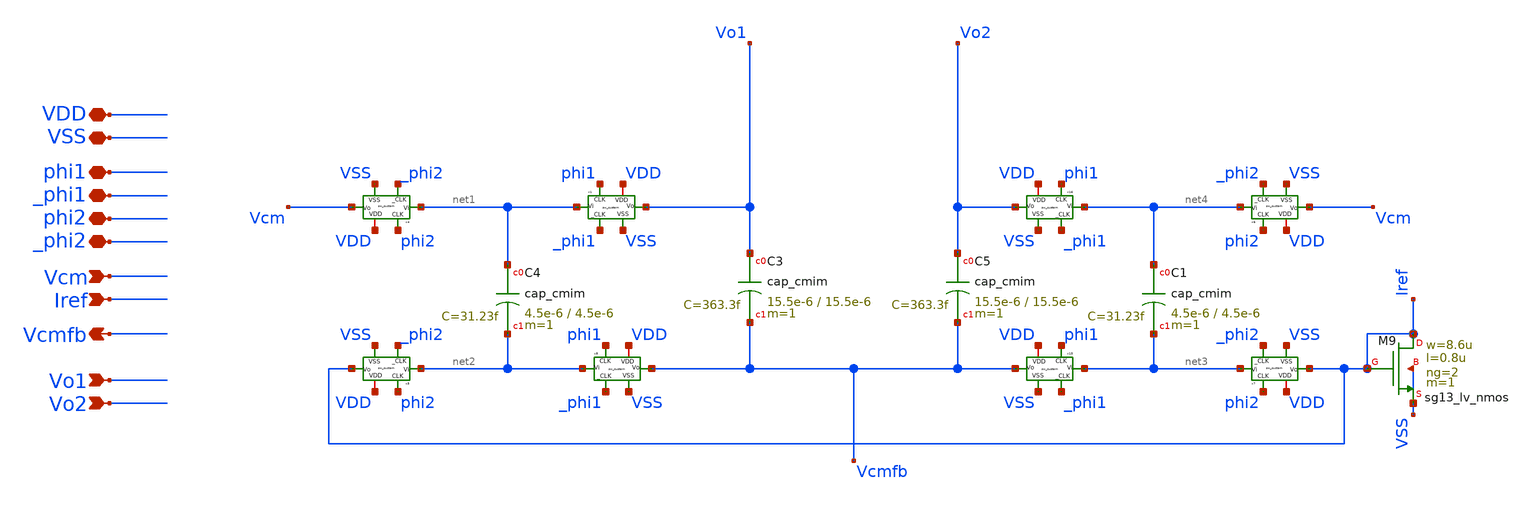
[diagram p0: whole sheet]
** sch_path: sch/blocks/cmfb.sch
**.subckt cmfb VDD VSS phi1 _phi1 phi2 _phi2 Vcm Iref Vcmfb Vo1 Vo2
*.iopin VDD
*.iopin VSS
*.iopin phi1
*.iopin _phi1
*.iopin phi2
*.iopin _phi2
*.ipin Vcm
*.ipin Iref
*.opin Vcmfb
*.ipin Vo1
*.ipin Vo2
x15 phi1 VSS Vcmfb net3 VDD _phi1 sw_custom
x16 phi1 VSS Vo2 net4 VDD _phi1 sw_custom
x1 phi1 VSS Vo1 net1 VDD _phi1 sw_custom
XM9 Iref Iref VSS VSS sg13_lv_nmos w=8.6u l=0.8u ng=2 m=1 mm_ok=1
x4 phi2 VSS Vcm net1 VDD _phi2 sw_custom
x5 phi2 VSS Iref net2 VDD _phi2 sw_custom
x6 phi2 VSS Vcm net4 VDD _phi2 sw_custom
x7 phi2 VSS Iref net3 VDD _phi2 sw_custom
x8 phi1 VSS Vcmfb net2 VDD _phi1 sw_custom
XC3 Vo1 Vcmfb cap_cmim w=15.5e-6 l=15.5e-6 m=1 mm_ok=1
XC4 net1 net2 cap_cmim w=4.5e-6 l=4.5e-6 m=1 mm_ok=1
XC5 Vo2 Vcmfb cap_cmim w=15.5e-6 l=15.5e-6 m=1 mm_ok=1
XC1 net4 net3 cap_cmim w=4.5e-6 l=4.5e-6 m=1 mm_ok=1
**.ends

* expanding   symbol:  sw_custom.sym # of pins=6
** sym_path: sch/blocks/sw_custom.sym
** sch_path: sch/blocks/sw_custom.sch
.subckt sw_custom CLK VSS Vo Vi VDD _CLK
*.iopin VSS
*.ipin CLK
*.ipin _CLK
*.iopin Vi
*.iopin Vo
*.iopin VDD
S1 Vi Vo CLK VSS SW1
.ends

**** begin user architecture code
.MODEL SW1 SW   VT=0.9 VH=0.01  RON=0.01 ROFF=10G
**** end user architecture code
.end
